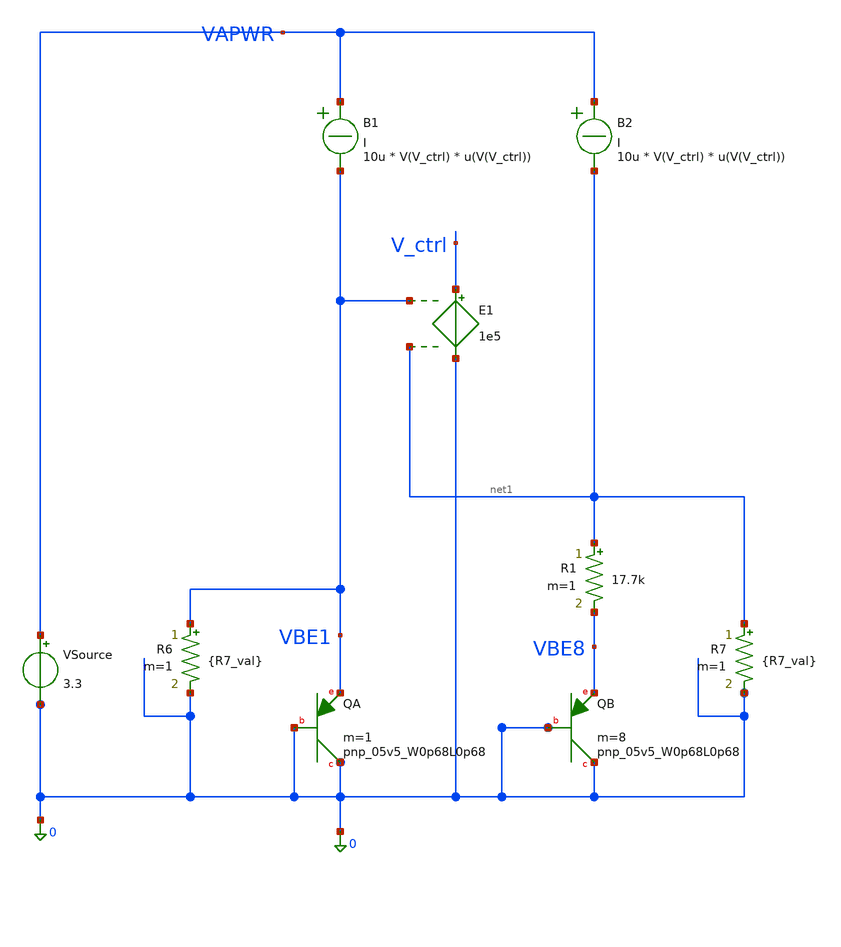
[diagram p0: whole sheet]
** sch_path: designs/bgr_ldo/sim/bgr_core_tb.sch
**.subckt bgr_core_tb
XQA 0 0 VBE1 sky130_fd_pr__pnp_05v5_W0p68L0p68 m=1
VSource VAPWR 0 3.3
XQB 0 0 VBE8 sky130_fd_pr__pnp_05v5_W0p68L0p68 m=8
R1 net1 VBE8 17.7k m=1
R7 net1 0 {R7_val} m=1
R6 VBE1 0 {R7_val} m=1
E1 V_ctrl 0 VBE1 net1 1e5
B1 VAPWR VBE1 I = 10u * V(V_ctrl) * u(V(V_ctrl))
B2 VAPWR net1 I = 10u * V(V_ctrl) * u(V(V_ctrl))
**** begin user architecture code

.nodeset v(vbe1)=0.88 v(net1)=0.88 v(v_ctrl)=1.5
.param R7_val=180k
.save all
.save @r1[i]
.save @r6[i]
.dc temp -40 125 5

.control
  let r_start = 110k
  let r_stop = 130k
  let r_step = 3k
  let r_curr = r_start

  while r_curr <= r_stop
    alterparam R7_val = $&r_curr
    reset
    nodeset v(vbe1)=0.88 v(net1)=0.88 v(v_ctrl)=1.5
    run
    let r_curr = r_curr + r_step
  end

  plot dc1.@r1[i]+dc1.@r6[i] dc2.@r1[i]+dc2.@r6[i] dc3.@r1[i]+dc3.@r6[i] dc4.@r1[i]+dc4.@r6[i]
+ dc5.@r1[i]+dc5.@r6[i] dc6.@r1[i]+dc6.@r6[i] dc7.@r1[i]+dc7.@r6[i]
.endc


** opencircuitdesign pdks install
.lib $::SKYWATER_MODELS/sky130.lib.spice tt

**** end user architecture code
**.ends
.end
